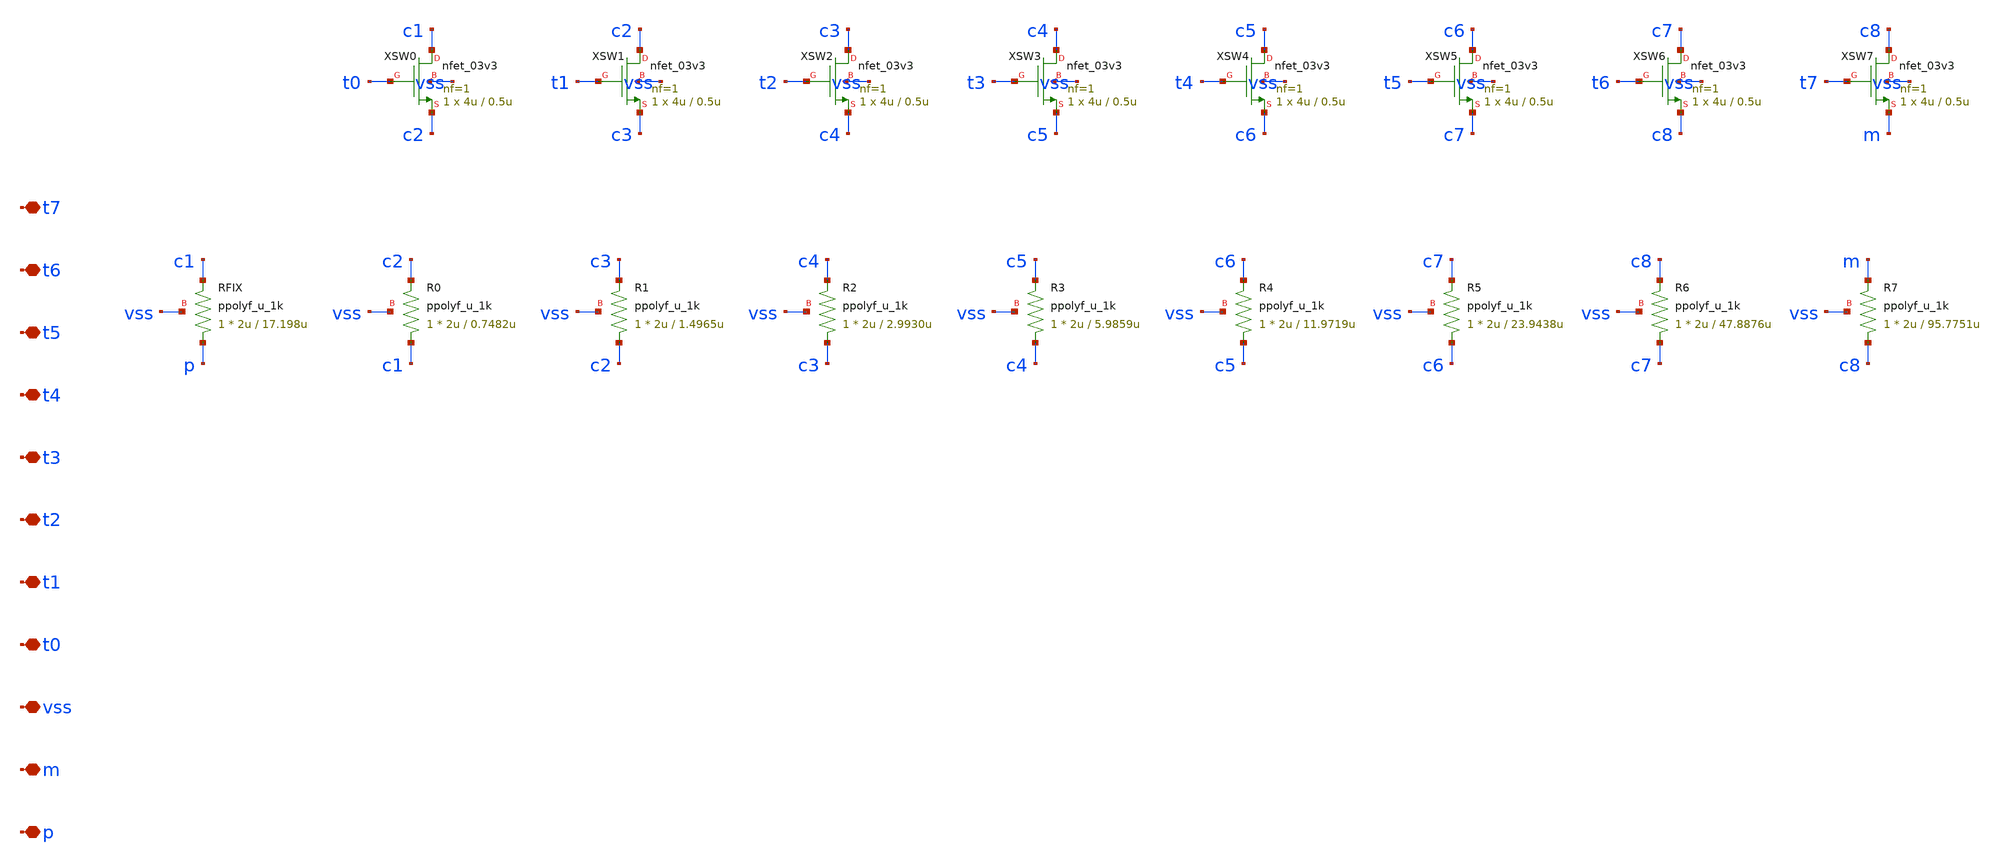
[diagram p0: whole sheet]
** sch_path: design/rcosc_trim_bank.sch
**.subckt rcosc_trim_bank p m vss t0 t1 t2 t3 t4 t5 t6 t7
*.iopin p
*.iopin m
*.iopin vss
*.iopin t0
*.iopin t1
*.iopin t2
*.iopin t3
*.iopin t4
*.iopin t5
*.iopin t6
*.iopin t7
XRFIX p c1 vss ppolyf_u_1k r_width=2u r_length=17.198u m=1
XR0 c1 c2 vss ppolyf_u_1k r_width=2u r_length=0.7482u m=1
XSW0 c1 t0 c2 vss nfet_03v3 L=0.5u W=4u nf=1 ad='int((nf+1)/2) * W/nf * 0.18u' as='int((nf+2)/2) * W/nf * 0.18u'
+ pd='2*int((nf+1)/2) * (W/nf + 0.18u)' ps='2*int((nf+2)/2) * (W/nf + 0.18u)' nrd='0.18u / W' nrs='0.18u / W'
+ sa=0 sb=0 sd=0 m=1
XR1 c2 c3 vss ppolyf_u_1k r_width=2u r_length=1.4965u m=1
XSW1 c2 t1 c3 vss nfet_03v3 L=0.5u W=4u nf=1 ad='int((nf+1)/2) * W/nf * 0.18u' as='int((nf+2)/2) * W/nf * 0.18u'
+ pd='2*int((nf+1)/2) * (W/nf + 0.18u)' ps='2*int((nf+2)/2) * (W/nf + 0.18u)' nrd='0.18u / W' nrs='0.18u / W'
+ sa=0 sb=0 sd=0 m=1
XR2 c3 c4 vss ppolyf_u_1k r_width=2u r_length=2.9930u m=1
XSW2 c3 t2 c4 vss nfet_03v3 L=0.5u W=4u nf=1 ad='int((nf+1)/2) * W/nf * 0.18u' as='int((nf+2)/2) * W/nf * 0.18u'
+ pd='2*int((nf+1)/2) * (W/nf + 0.18u)' ps='2*int((nf+2)/2) * (W/nf + 0.18u)' nrd='0.18u / W' nrs='0.18u / W'
+ sa=0 sb=0 sd=0 m=1
XR3 c4 c5 vss ppolyf_u_1k r_width=2u r_length=5.9859u m=1
XSW3 c4 t3 c5 vss nfet_03v3 L=0.5u W=4u nf=1 ad='int((nf+1)/2) * W/nf * 0.18u' as='int((nf+2)/2) * W/nf * 0.18u'
+ pd='2*int((nf+1)/2) * (W/nf + 0.18u)' ps='2*int((nf+2)/2) * (W/nf + 0.18u)' nrd='0.18u / W' nrs='0.18u / W'
+ sa=0 sb=0 sd=0 m=1
XR4 c5 c6 vss ppolyf_u_1k r_width=2u r_length=11.9719u m=1
XSW4 c5 t4 c6 vss nfet_03v3 L=0.5u W=4u nf=1 ad='int((nf+1)/2) * W/nf * 0.18u' as='int((nf+2)/2) * W/nf * 0.18u'
+ pd='2*int((nf+1)/2) * (W/nf + 0.18u)' ps='2*int((nf+2)/2) * (W/nf + 0.18u)' nrd='0.18u / W' nrs='0.18u / W'
+ sa=0 sb=0 sd=0 m=1
XR5 c6 c7 vss ppolyf_u_1k r_width=2u r_length=23.9438u m=1
XSW5 c6 t5 c7 vss nfet_03v3 L=0.5u W=4u nf=1 ad='int((nf+1)/2) * W/nf * 0.18u' as='int((nf+2)/2) * W/nf * 0.18u'
+ pd='2*int((nf+1)/2) * (W/nf + 0.18u)' ps='2*int((nf+2)/2) * (W/nf + 0.18u)' nrd='0.18u / W' nrs='0.18u / W'
+ sa=0 sb=0 sd=0 m=1
XR6 c7 c8 vss ppolyf_u_1k r_width=2u r_length=47.8876u m=1
XSW6 c7 t6 c8 vss nfet_03v3 L=0.5u W=4u nf=1 ad='int((nf+1)/2) * W/nf * 0.18u' as='int((nf+2)/2) * W/nf * 0.18u'
+ pd='2*int((nf+1)/2) * (W/nf + 0.18u)' ps='2*int((nf+2)/2) * (W/nf + 0.18u)' nrd='0.18u / W' nrs='0.18u / W'
+ sa=0 sb=0 sd=0 m=1
XR7 c8 m vss ppolyf_u_1k r_width=2u r_length=95.7751u m=1
XSW7 c8 t7 m vss nfet_03v3 L=0.5u W=4u nf=1 ad='int((nf+1)/2) * W/nf * 0.18u' as='int((nf+2)/2) * W/nf * 0.18u'
+ pd='2*int((nf+1)/2) * (W/nf + 0.18u)' ps='2*int((nf+2)/2) * (W/nf + 0.18u)' nrd='0.18u / W' nrs='0.18u / W'
+ sa=0 sb=0 sd=0 m=1
**.ends
.end
